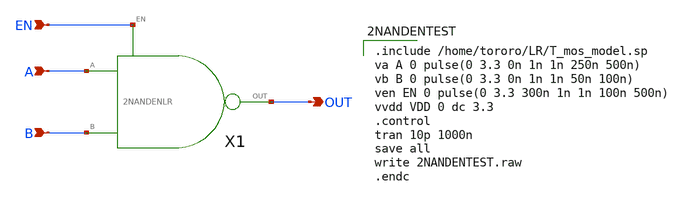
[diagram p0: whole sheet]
** sch_path: task_LATCH/2NANDENTEST.sch
**.subckt 2NANDENTEST A B OUT EN
*.ipin A
*.ipin B
*.opin OUT
*.ipin EN
X1 A B OUT EN 2NANDENLR
**** begin user architecture code

.include /home/tororo/LR/T_mos_model.sp
va A 0 pulse(0 3.3 0n 1n 1n 250n 500n)
vb B 0 pulse(0 3.3 0n 1n 1n 50n 100n)
ven EN 0 pulse(0 3.3 300n 1n 1n 100n 500n)
vvdd VDD 0 dc 3.3
.control
tran 10p 1000n
save all
write 2NANDENTEST.raw
.endc

**** end user architecture code
**.ends

* expanding   symbol:  LR/2NANDENLR.sym # of pins=4
** sym_path: task_LATCH/2NANDENLR.sym
** sch_path: task_LATCH/2NANDENLR.sch
.subckt 2NANDENLR A B OUT EN
*.ipin A
*.ipin B
*.opin OUT
*.ipin EN
M1 OUT A net1 GND nch w=3.5u l=0.35u as=0 ps=0 ad=0 pd=0 m=1
M2 OUT B VDDL VDDL pch w=3.5u l=0.35u as=0 ps=0 ad=0 pd=0 m=1
M3 OUT A VDDL VDDL pch w=3.5u l=0.35u as=0 ps=0 ad=0 pd=0 m=1
M4 net1 B GND GND nch w=3.5u l=0.35u as=0 ps=0 ad=0 pd=0 m=1
M5 VDDL EN VDD VDD pch w=3.5u l=0.35u as=0 ps=0 ad=0 pd=0 m=1
**** begin user architecture code

.include /home/tororo/LR/T_mos_model.sp
va A 0 pulse(0 3.3 0n 1n 1n 250n 500n)
vb B 0 pulse(0 3.3 0n 1n 1n 50n 100n)
ven EN 0 pulse(0 3.3 300n 1n 1n 100n 500n)
vvdd VDD 0 dc 3.3
.control
tran 10p 1000n
save all
write 2NANDENLR.raw
.endc

**** end user architecture code
.ends

.GLOBAL VDD
.GLOBAL GND
.end
